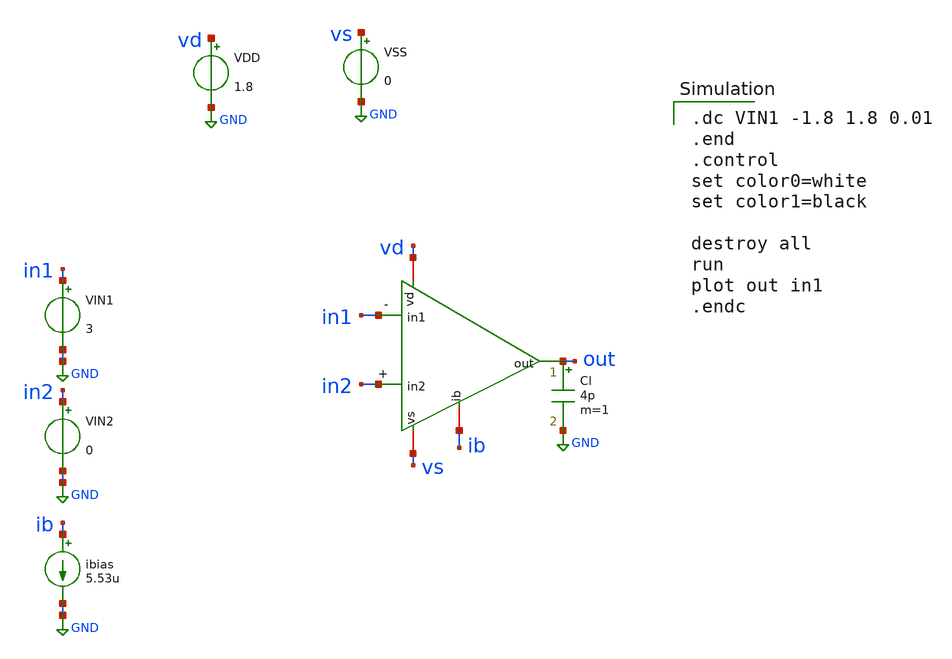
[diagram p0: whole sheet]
** sch_path: amp-op/xschem/ampop_tb-dc.sch
* Copyright 2020 Stefan Frederik Schippers
* Licensed under the Apache License, Version 2.0 (the "License");
* you may not use this file except in compliance with the License.
* You may obtain a copy of the License at
* https://www.apache.org/licenses/LICENSE-2.0
* Unless required by applicable law or agreed to in writing, software
* distributed under the License is distributed on an "AS IS" BASIS,
* WITHOUT WARRANTIES OR CONDITIONS OF ANY KIND, either express or implied.
* See the License for the specific language governing permissions and
* limitations under the License.
**.subckt ampop_tb-dc
VIN2 in2 GND 0
VIN1 in1 GND 3
ibias ib GND 5.53u
VDD vd GND 1.8
VSS vs GND 0
Cl out GND 4p m=1
x1 vd in1 in2 out ib vs ampop
**** begin user architecture code

.dc VIN1 -1.8 1.8 0.01
.end
.control
set color0=white
set color1=black

destroy all
run
plot out in1
.endc

 .lib $::SKYWATER_MODELS/sky130.lib.spice tt
.include $::SKYWATER_STDCELLS/sky130_fd_sc_hd.spice

**** end user architecture code
**.ends
.GLOBAL GND
.end
